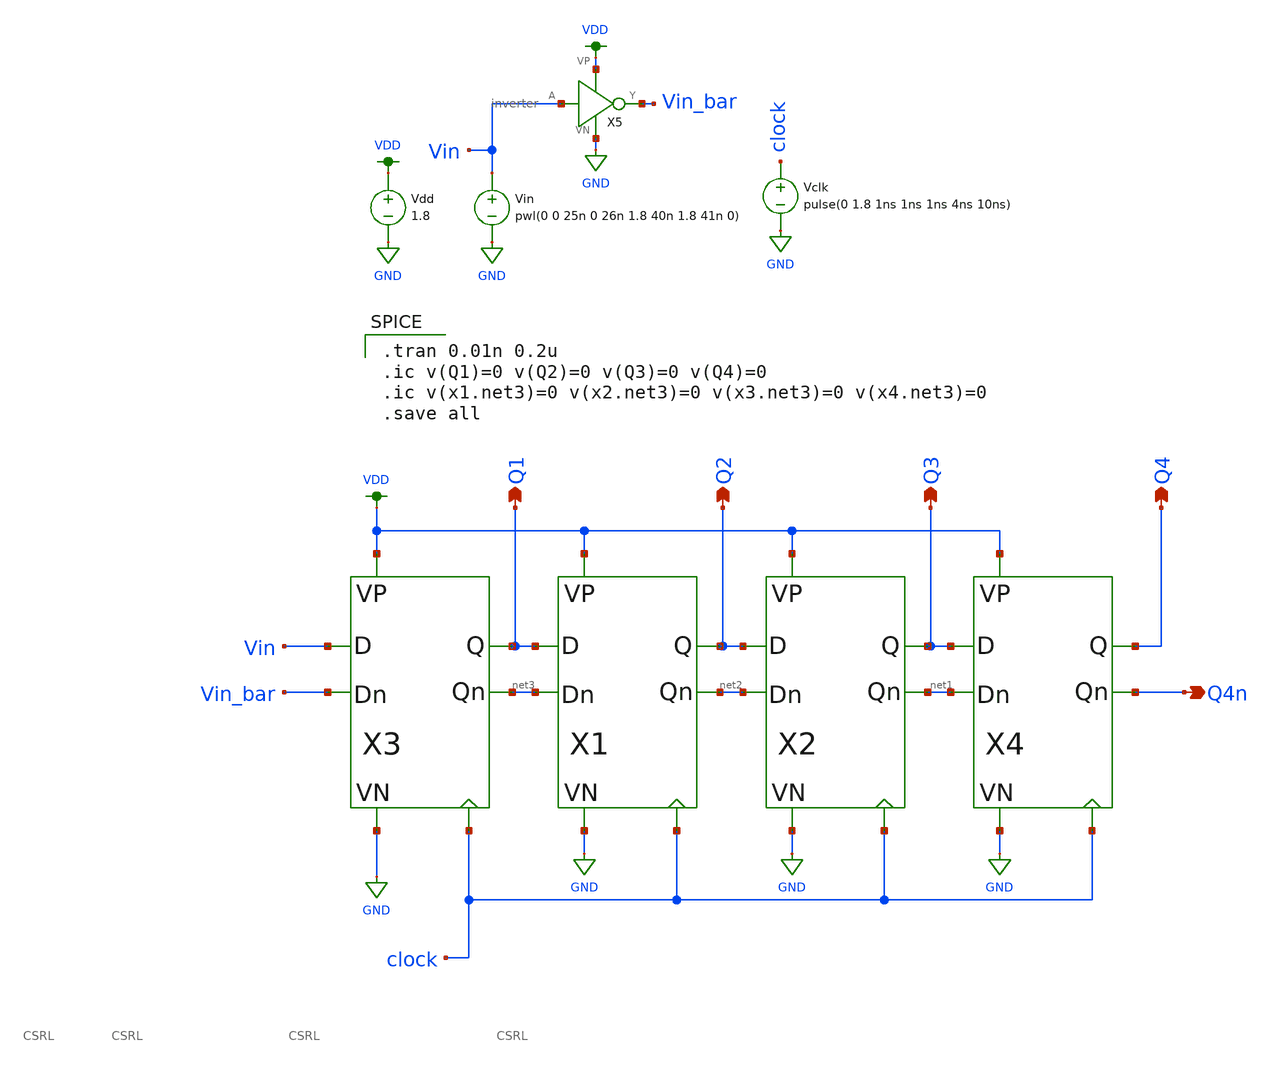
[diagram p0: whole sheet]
** sch_path: shiftreg_test.sch
**.subckt shiftreg_test Q1 Q2 Q3 Q4 Q4n
*.opin Q1
*.opin Q2
*.opin Q3
*.opin Q4
*.opin Q4n
X3 Vin Vin_bar VDD GND net3 Q1 clock CSRL
X1 Q1 net3 VDD GND net2 Q2 clock CSRL
X2 Q2 net2 VDD GND net1 Q3 clock CSRL
X4 Q3 net1 VDD GND Q4n Q4 clock CSRL
X5 Vin Vin_bar VDD GND inverter
Vdd VDD GND 1.8
Vin Vin GND pwl(0 0 25n 0 26n 1.8 40n 1.8 41n 0)
Vclk clock GND pulse(0 1.8 1ns 1ns 1ns 4ns 10ns)
**** begin user architecture code

.tran 0.01n 0.2u
.ic v(Q1)=0 v(Q2)=0 v(Q3)=0 v(Q4)=0
.ic v(x1.net3)=0 v(x2.net3)=0 v(x3.net3)=0 v(x4.net3)=0
.save all


.option wnflag=1
.lib ~/skywater/skywater-pdk/libraries/sky130_fd_pr_ngspice/latest/models/sky130.lib.spice tt

**** end user architecture code
**.ends

* expanding   symbol:  /home/jonah/VLSI/MP2/CSRL.sym # of pins=7
** sym_path: CSRL.sym
** sch_path: CSRL.sch
.subckt CSRL D Dn VP VN Qn Q CLK
*.ipin CLK
*.iopin VN
*.iopin VP
*.iopin D
*.iopin Dn
*.iopin Q
*.iopin Qn
XM1 net1 CLK VN GND sky130_fd_pr__nfet_01v8 L=0.15 W=1 nf=1 ad='int((nf+1)/2) * W/nf * 0.29' as='int((nf+2)/2) * W/nf * 0.29'
+ pd='2*int((nf+1)/2) * (W/nf + 0.29)' ps='2*int((nf+2)/2) * (W/nf + 0.29)' nrd='0.29 / W' nrs='0.29 / W'
+ sa=0 sb=0 sd=0 mult=1 m=1
XM2 net1 net2 net3 GND sky130_fd_pr__nfet_01v8 L=0.15 W=1 nf=1 ad='int((nf+1)/2) * W/nf * 0.29' as='int((nf+2)/2) * W/nf * 0.29'
+ pd='2*int((nf+1)/2) * (W/nf + 0.29)' ps='2*int((nf+2)/2) * (W/nf + 0.29)' nrd='0.29 / W' nrs='0.29 / W'
+ sa=0 sb=0 sd=0 mult=1 m=1
XM3 net1 net3 net2 GND sky130_fd_pr__nfet_01v8 L=0.15 W=1 nf=1 ad='int((nf+1)/2) * W/nf * 0.29' as='int((nf+2)/2) * W/nf * 0.29'
+ pd='2*int((nf+1)/2) * (W/nf + 0.29)' ps='2*int((nf+2)/2) * (W/nf + 0.29)' nrd='0.29 / W' nrs='0.29 / W'
+ sa=0 sb=0 sd=0 mult=1 m=1
XM4 Qn CLK net2 GND sky130_fd_pr__nfet_01v8 L=0.15*4 W=1 nf=1 ad='int((nf+1)/2) * W/nf * 0.29' as='int((nf+2)/2) * W/nf * 0.29'
+ pd='2*int((nf+1)/2) * (W/nf + 0.29)' ps='2*int((nf+2)/2) * (W/nf + 0.29)' nrd='0.29 / W' nrs='0.29 / W'
+ sa=0 sb=0 sd=0 mult=1 m=1
XM5 Q CLK net3 GND sky130_fd_pr__nfet_01v8 L=0.15*4 W=1 nf=1 ad='int((nf+1)/2) * W/nf * 0.29' as='int((nf+2)/2) * W/nf * 0.29'
+ pd='2*int((nf+1)/2) * (W/nf + 0.29)' ps='2*int((nf+2)/2) * (W/nf + 0.29)' nrd='0.29 / W' nrs='0.29 / W'
+ sa=0 sb=0 sd=0 mult=1 m=1
XM6 VN Q Qn GND sky130_fd_pr__nfet_01v8 L=0.15 W=1 nf=1 ad='int((nf+1)/2) * W/nf * 0.29' as='int((nf+2)/2) * W/nf * 0.29'
+ pd='2*int((nf+1)/2) * (W/nf + 0.29)' ps='2*int((nf+2)/2) * (W/nf + 0.29)' nrd='0.29 / W' nrs='0.29 / W'
+ sa=0 sb=0 sd=0 mult=1 m=1
XM7 VN Qn Q GND sky130_fd_pr__nfet_01v8 L=0.15 W=1 nf=1 ad='int((nf+1)/2) * W/nf * 0.29' as='int((nf+2)/2) * W/nf * 0.29'
+ pd='2*int((nf+1)/2) * (W/nf + 0.29)' ps='2*int((nf+2)/2) * (W/nf + 0.29)' nrd='0.29 / W' nrs='0.29 / W'
+ sa=0 sb=0 sd=0 mult=1 m=1
XM8 net2 net3 VP VDD sky130_fd_pr__pfet_01v8 L=0.15 W=1 nf=1 ad='int((nf+1)/2) * W/nf * 0.29' as='int((nf+2)/2) * W/nf * 0.29'
+ pd='2*int((nf+1)/2) * (W/nf + 0.29)' ps='2*int((nf+2)/2) * (W/nf + 0.29)' nrd='0.29 / W' nrs='0.29 / W'
+ sa=0 sb=0 sd=0 mult=1 m=1
XM9 net2 CLK Dn VDD sky130_fd_pr__pfet_01v8 L=0.15*4 W=1 nf=1 ad='int((nf+1)/2) * W/nf * 0.29' as='int((nf+2)/2) * W/nf * 0.29'
+ pd='2*int((nf+1)/2) * (W/nf + 0.29)' ps='2*int((nf+2)/2) * (W/nf + 0.29)' nrd='0.29 / W' nrs='0.29 / W'
+ sa=0 sb=0 sd=0 mult=1 m=1
XM10 net3 net2 VP VDD sky130_fd_pr__pfet_01v8 L=0.15 W=1 nf=1 ad='int((nf+1)/2) * W/nf * 0.29' as='int((nf+2)/2) * W/nf * 0.29'
+ pd='2*int((nf+1)/2) * (W/nf + 0.29)' ps='2*int((nf+2)/2) * (W/nf + 0.29)' nrd='0.29 / W' nrs='0.29 / W'
+ sa=0 sb=0 sd=0 mult=1 m=1
XM11 net3 CLK D VDD sky130_fd_pr__pfet_01v8 L=0.15*4 W=1 nf=1 ad='int((nf+1)/2) * W/nf * 0.29' as='int((nf+2)/2) * W/nf * 0.29'
+ pd='2*int((nf+1)/2) * (W/nf + 0.29)' ps='2*int((nf+2)/2) * (W/nf + 0.29)' nrd='0.29 / W' nrs='0.29 / W'
+ sa=0 sb=0 sd=0 mult=1 m=1
XM12 net4 CLK VP VDD sky130_fd_pr__pfet_01v8 L=0.15 W=1 nf=1 ad='int((nf+1)/2) * W/nf * 0.29' as='int((nf+2)/2) * W/nf * 0.29'
+ pd='2*int((nf+1)/2) * (W/nf + 0.29)' ps='2*int((nf+2)/2) * (W/nf + 0.29)' nrd='0.29 / W' nrs='0.29 / W'
+ sa=0 sb=0 sd=0 mult=1 m=1
XM13 Q Qn net4 VDD sky130_fd_pr__pfet_01v8 L=0.15 W=1 nf=1 ad='int((nf+1)/2) * W/nf * 0.29' as='int((nf+2)/2) * W/nf * 0.29'
+ pd='2*int((nf+1)/2) * (W/nf + 0.29)' ps='2*int((nf+2)/2) * (W/nf + 0.29)' nrd='0.29 / W' nrs='0.29 / W'
+ sa=0 sb=0 sd=0 mult=1 m=1
XM14 Qn Q net4 VDD sky130_fd_pr__pfet_01v8 L=0.15 W=1 nf=1 ad='int((nf+1)/2) * W/nf * 0.29' as='int((nf+2)/2) * W/nf * 0.29'
+ pd='2*int((nf+1)/2) * (W/nf + 0.29)' ps='2*int((nf+2)/2) * (W/nf + 0.29)' nrd='0.29 / W' nrs='0.29 / W'
+ sa=0 sb=0 sd=0 mult=1 m=1
.ends


* expanding   symbol:  /home/jonah/VLSI/MP1/inverter.sym # of pins=4
** sym_path: /home/jonah/VLSI/MP1/inverter.sym
** sch_path: /home/jonah/VLSI/MP1/inverter.sch
.subckt inverter A Y VP VN
*.ipin A
*.iopin VP
*.iopin VN
*.iopin Y
XM1 Y A VN VN sky130_fd_pr__nfet_01v8 L=0.15 W=1 nf=1 ad='int((nf+1)/2) * W/nf * 0.29' as='int((nf+2)/2) * W/nf * 0.29'
+ pd='2*int((nf+1)/2) * (W/nf + 0.29)' ps='2*int((nf+2)/2) * (W/nf + 0.29)' nrd='0.29 / W' nrs='0.29 / W'
+ sa=0 sb=0 sd=0 mult=1 m=1
XM2 Y A VP VP sky130_fd_pr__pfet_01v8 L=0.15 W=1 nf=1 ad='int((nf+1)/2) * W/nf * 0.29' as='int((nf+2)/2) * W/nf * 0.29'
+ pd='2*int((nf+1)/2) * (W/nf + 0.29)' ps='2*int((nf+2)/2) * (W/nf + 0.29)' nrd='0.29 / W' nrs='0.29 / W'
+ sa=0 sb=0 sd=0 mult=1 m=1
.ends

.GLOBAL GND
.GLOBAL VDD
.end
